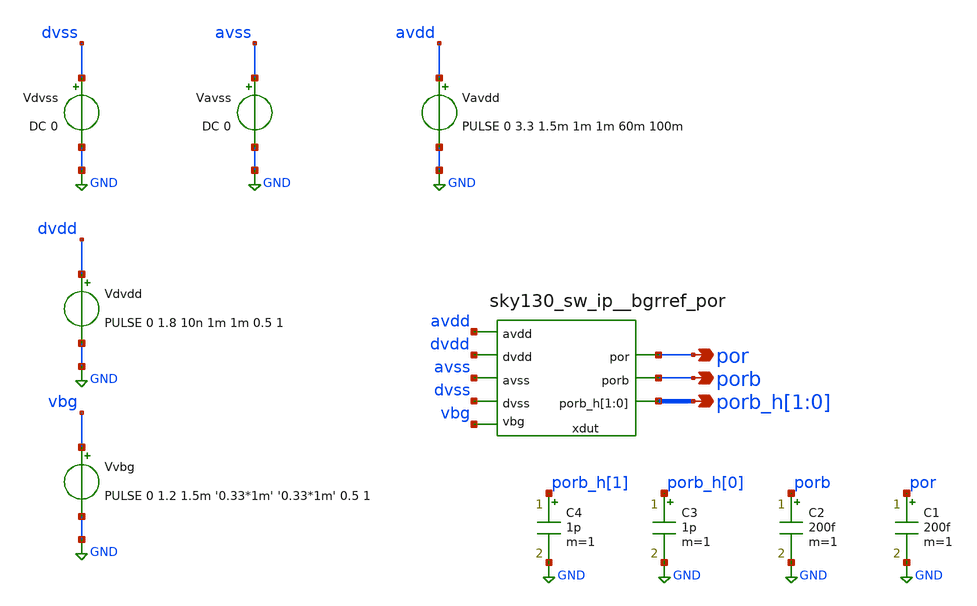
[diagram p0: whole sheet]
** sch_path: cace/templates/temp/por_hys_temp.sch
**.subckt por_hys_temp por porb porb_h[1],porb_h[0]
*.opin por
*.opin porb
*.opin porb_h[1],porb_h[0]
Vdvss dvss GND DC 0
Vavdd avdd GND PULSE 0 3.3 1.5m 1m 1m 60m 100m
Vavss avss GND DC 0
Vdvdd dvdd GND PULSE 0 1.8 10n 1m 1m 0.5 1
Vvbg vbg GND PULSE 0 1.2 1.5m '0.33*1m' '0.33*1m' 0.5 1
xdut vbg por avss avdd dvdd porb dvss porb_h[1] porb_h[0] sky130_sw_ip__bgrref_por
C1 por GND 200f m=1
C2 porb GND 200f m=1
C3 porb_h[0] GND 1p m=1
C4 porb_h[1] GND 1p m=1
**** begin user architecture code


*.include /home/efabless/analog_ip/cheetah_v3_analog/dependencies/sky130_sw_ip__bgrref_por/netlist/rcx/sky130_sw_ip__bgrref_por.spice
.options savecurrents
.control
save all
let Tsimend = 120m + 2*1m
tran 1u $&Tsimend
let dvdd_half = 0.5*1.8
let meas_window = 0.001 + 3.5m
meas tran V_thp FIND v(avdd) When v(xdut.rst)=dvdd_half FROM=0 TO=meas_window RISE=LAST
meas tran V_thn FIND v(avdd) WHEN V(xdut.rst)=dvdd_half TD=meas_window FALL=LAST
let hyst='V_thp-V_thn'
write sky130_sw_ip__bgrref_por_tb1.raw
print hyst
*quit
.endc


 .lib $::SKYWATER_MODELS/sky130.lib.spice tt

.include $::SKYWATER_STDCELLS/sky130_fd_sc_hd.spice
.include $::SKYWATER_STDCELLS/../../sky130_fd_sc_hvl/spice/sky130_fd_sc_hvl.spice
.include $::SKYWATER_STDCELLS/../../sky130_fd_sc_ls/spice/sky130_fd_sc_ls.spice


**** end user architecture code
**.ends
.GLOBAL GND
.end
